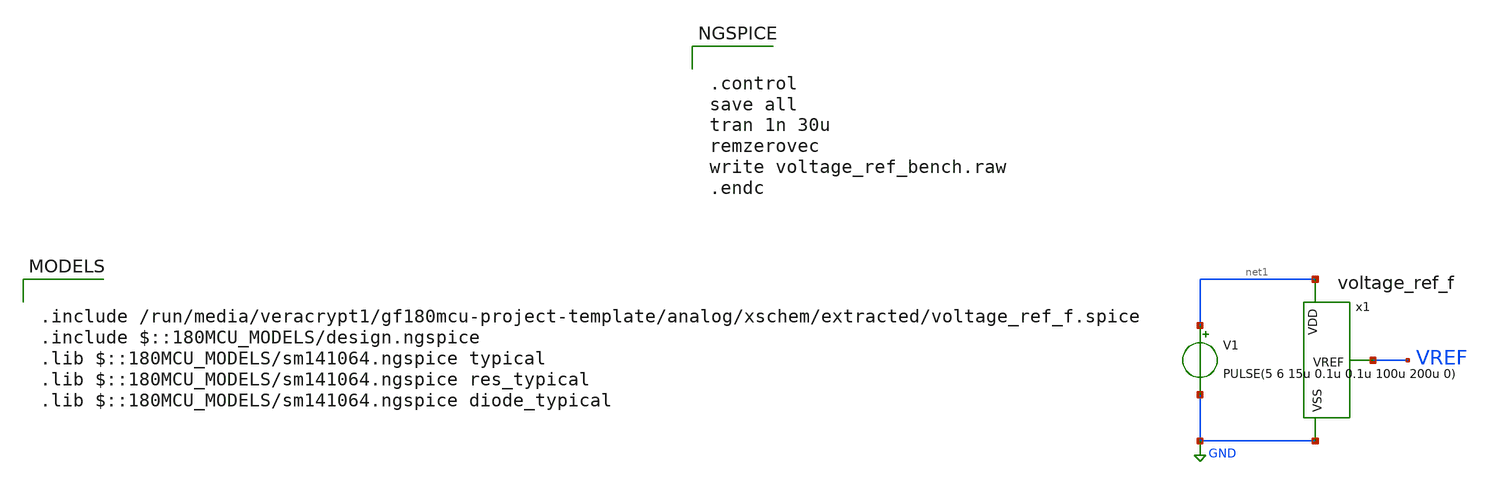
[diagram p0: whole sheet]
** sch_path: analog/xschem/voltage_ref_bench.sch
**.subckt voltage_ref_bench
V1 net1 GND PULSE(5 6 15u 0.1u 0.1u 100u 200u 0)
x1 net1 GND VREF voltage_ref_f
**** begin user architecture code


.control
save all
tran 1n 30u
remzerovec
write voltage_ref_bench.raw
.endc



.include /run/media/veracrypt1/gf180mcu-project-template/analog/xschem/extracted/voltage_ref_f.spice
.include $::180MCU_MODELS/design.ngspice
.lib $::180MCU_MODELS/sm141064.ngspice typical
.lib $::180MCU_MODELS/sm141064.ngspice res_typical
.lib $::180MCU_MODELS/sm141064.ngspice diode_typical

**** end user architecture code
**.ends
.GLOBAL GND
.end
